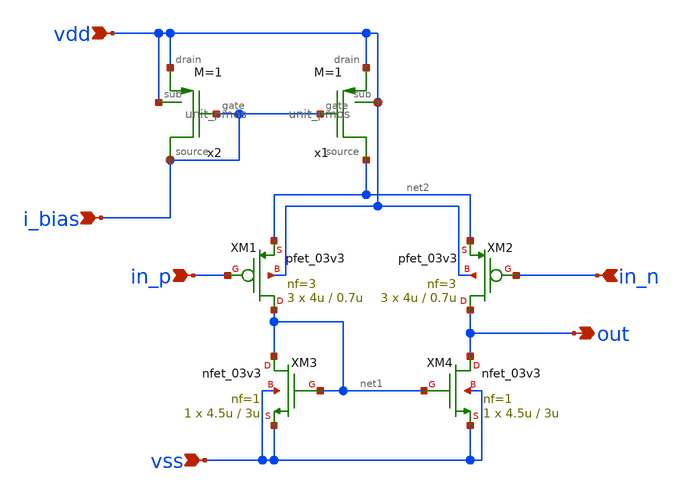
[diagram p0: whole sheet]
** sch_path: designs/switch_matrix_gf180mcu_9t5v0-main/designs/libs/core_analog/ota_5t/ota_5t_P.sch
**.subckt ota_5t_P in_n i_bias vdd vss out in_p
*.ipin in_n
*.ipin i_bias
*.ipin vdd
*.ipin vss
*.opin out
*.ipin in_p
XM4 out net1 vss vss nfet_03v3 L=3u W=4.5u nf=1 ad='int((nf+1)/2) * W/nf * 0.18u' as='int((nf+2)/2) * W/nf * 0.18u'
+ pd='2*int((nf+1)/2) * (W/nf + 0.18u)' ps='2*int((nf+2)/2) * (W/nf + 0.18u)' nrd='0.18u / W' nrs='0.18u / W'
+ sa=0 sb=0 sd=0 m=1
XM3 net1 net1 vss vss nfet_03v3 L=3u W=4.5u nf=1 ad='int((nf+1)/2) * W/nf * 0.18u' as='int((nf+2)/2) * W/nf * 0.18u'
+ pd='2*int((nf+1)/2) * (W/nf + 0.18u)' ps='2*int((nf+2)/2) * (W/nf + 0.18u)' nrd='0.18u / W' nrs='0.18u / W'
+ sa=0 sb=0 sd=0 m=1
XM2 out in_n net2 vdd pfet_03v3 L=0.7u W=4u nf=3 ad='int((nf+1)/2) * W/nf * 0.18u' as='int((nf+2)/2) * W/nf * 0.18u'
+ pd='2*int((nf+1)/2) * (W/nf + 0.18u)' ps='2*int((nf+2)/2) * (W/nf + 0.18u)' nrd='0.18u / W' nrs='0.18u / W'
+ sa=0 sb=0 sd=0 m=3
XM1 net1 in_p net2 vdd pfet_03v3 L=0.7u W=4u nf=3 ad='int((nf+1)/2) * W/nf * 0.18u' as='int((nf+2)/2) * W/nf * 0.18u'
+ pd='2*int((nf+1)/2) * (W/nf + 0.18u)' ps='2*int((nf+2)/2) * (W/nf + 0.18u)' nrd='0.18u / W' nrs='0.18u / W'
+ sa=0 sb=0 sd=0 m=3
x2 vdd vdd i_bias i_bias unit_pmos M=1
x1 vdd vdd i_bias net2 unit_pmos M=1
**.ends
.end
